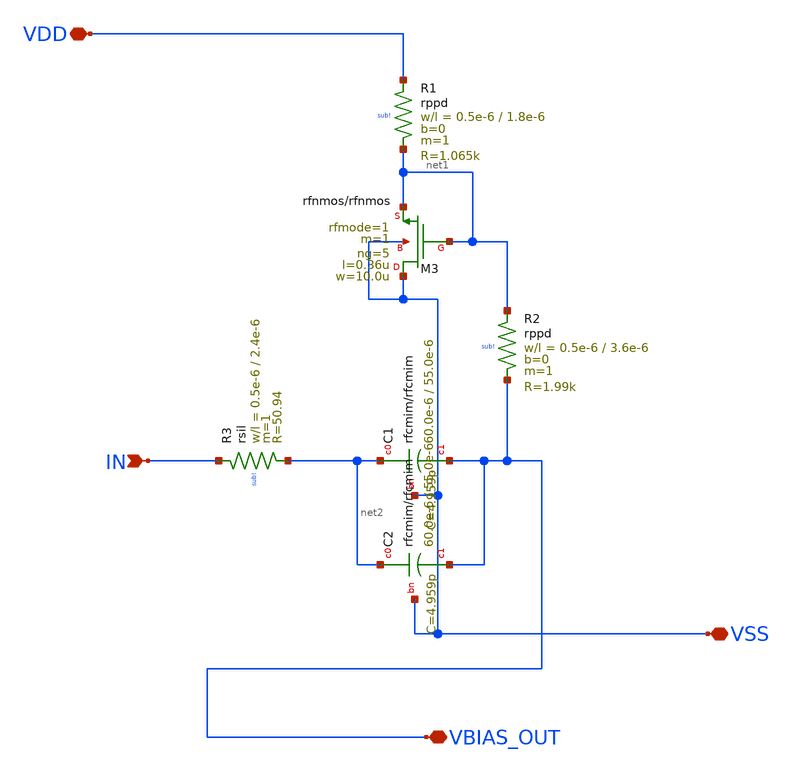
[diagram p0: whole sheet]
** sch_path: GPS_LNA/design_data/lvs/parts/vbias_inp.sch
**.subckt vbias_inp VDD IN VSS VBIAS_OUT
*.iopin VDD
*.ipin IN
*.iopin VSS
*.iopin VBIAS_OUT
XR2 net1 VBIAS_OUT sub! rppd w=0.5e-6 l=3.6e-6 m=1 b=0 mm_ok=1
XR1 VDD net1 sub! rppd w=0.5e-6 l=1.8e-6 m=1 b=0 mm_ok=1
XR3 IN net2 sub! rsil w=0.5e-6 l=2.4e-6 m=1 mm_ok=1
XC1 net2 VBIAS_OUT VSS rfcmim w=60.0e-6 l=55.0e-6 wfeed=5.0e-6 m=1 mm_ok=1
XC2 net2 VBIAS_OUT VSS rfcmim w=60.0e-6 l=55.0e-6 wfeed=5.0e-6 m=1 mm_ok=1
XM3 VSS net1 net1 VSS rfnmos w=10.0u l=0.36u ng=5 m=1 rfmode=1 mm_ok=1
**.ends
.end
